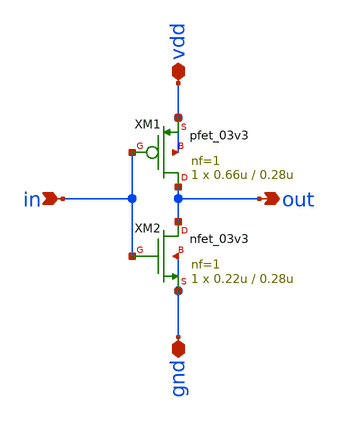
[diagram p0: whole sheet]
** sch_path: designs/libs/core_analog/two_stage_ota/inv.sch
**.subckt inv out in vdd gnd
*.opin out
*.ipin in
*.iopin vdd
*.iopin gnd
XM1 out in vdd vdd pfet_03v3 L=0.28u W=0.66u nf=1 ad='int((nf+1)/2) * W/nf * 0.18u' as='int((nf+2)/2) * W/nf * 0.18u'
+ pd='2*int((nf+1)/2) * (W/nf + 0.18u)' ps='2*int((nf+2)/2) * (W/nf + 0.18u)' nrd='0.18u / W' nrs='0.18u / W'
+ sa=0 sb=0 sd=0 m=1
XM2 out in gnd gnd nfet_03v3 L=0.28u W=0.22u nf=1 ad='int((nf+1)/2) * W/nf * 0.18u' as='int((nf+2)/2) * W/nf * 0.18u'
+ pd='2*int((nf+1)/2) * (W/nf + 0.18u)' ps='2*int((nf+2)/2) * (W/nf + 0.18u)' nrd='0.18u / W' nrs='0.18u / W'
+ sa=0 sb=0 sd=0 m=1
**.ends
.end
